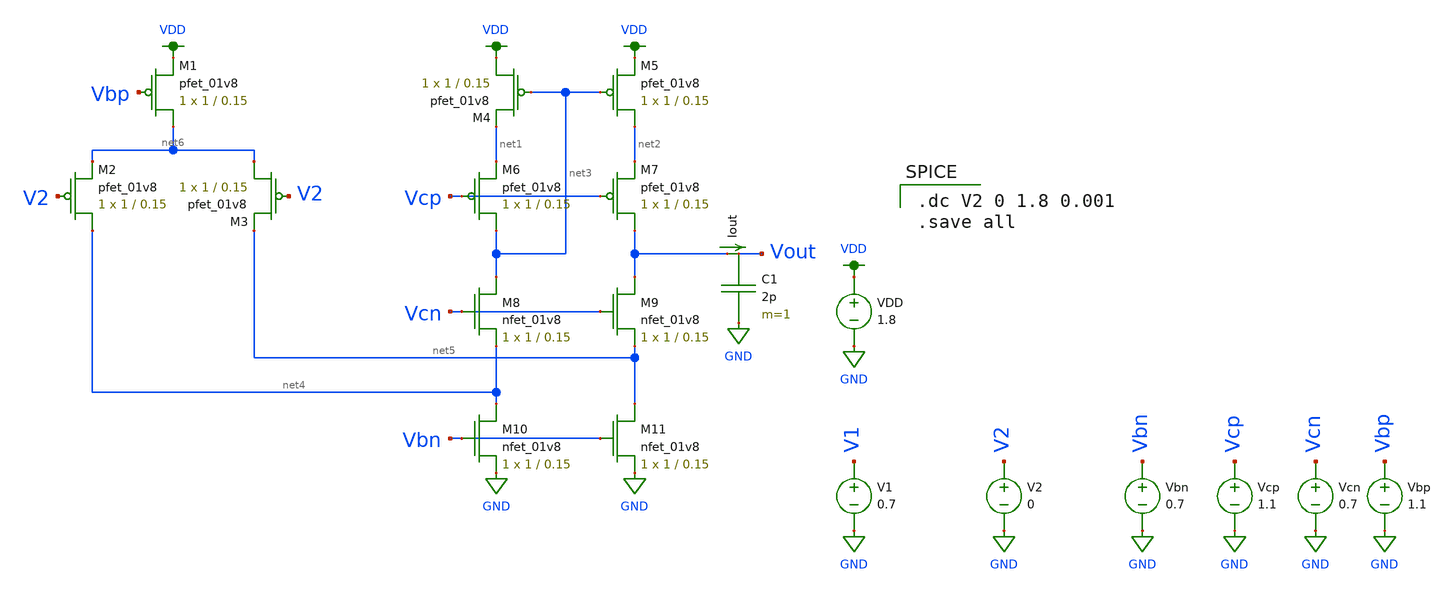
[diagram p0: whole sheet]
** sch_path: schematic/folded_cascode_differential_amplifier (copy).sch
**.subckt folded_cascode_differential_amplifier (copy)
XM1 net6 Vbp VDD VDD sky130_fd_pr__pfet_01v8 L=0.15 W=1 nf=1 ad='int((nf+1)/2) * W/nf * 0.29' as='int((nf+2)/2) * W/nf * 0.29'
+ pd='2*int((nf+1)/2) * (W/nf + 0.29)' ps='2*int((nf+2)/2) * (W/nf + 0.29)' nrd='0.29 / W' nrs='0.29 / W'
+ sa=0 sb=0 sd=0 mult=1 m=1
XM2 net4 V2 net6 VDD sky130_fd_pr__pfet_01v8 L=0.15 W=1 nf=1 ad='int((nf+1)/2) * W/nf * 0.29' as='int((nf+2)/2) * W/nf * 0.29'
+ pd='2*int((nf+1)/2) * (W/nf + 0.29)' ps='2*int((nf+2)/2) * (W/nf + 0.29)' nrd='0.29 / W' nrs='0.29 / W'
+ sa=0 sb=0 sd=0 mult=1 m=1
XM3 net6 V2 net5 VDD sky130_fd_pr__pfet_01v8 L=0.15 W=1 nf=1 ad='int((nf+1)/2) * W/nf * 0.29' as='int((nf+2)/2) * W/nf * 0.29'
+ pd='2*int((nf+1)/2) * (W/nf + 0.29)' ps='2*int((nf+2)/2) * (W/nf + 0.29)' nrd='0.29 / W' nrs='0.29 / W'
+ sa=0 sb=0 sd=0 mult=1 m=1
XM4 VDD net3 net1 VDD sky130_fd_pr__pfet_01v8 L=0.15 W=1 nf=1 ad='int((nf+1)/2) * W/nf * 0.29' as='int((nf+2)/2) * W/nf * 0.29'
+ pd='2*int((nf+1)/2) * (W/nf + 0.29)' ps='2*int((nf+2)/2) * (W/nf + 0.29)' nrd='0.29 / W' nrs='0.29 / W'
+ sa=0 sb=0 sd=0 mult=1 m=1
XM5 net2 net3 VDD VDD sky130_fd_pr__pfet_01v8 L=0.15 W=1 nf=1 ad='int((nf+1)/2) * W/nf * 0.29' as='int((nf+2)/2) * W/nf * 0.29'
+ pd='2*int((nf+1)/2) * (W/nf + 0.29)' ps='2*int((nf+2)/2) * (W/nf + 0.29)' nrd='0.29 / W' nrs='0.29 / W'
+ sa=0 sb=0 sd=0 mult=1 m=1
XM6 net3 Vcp net1 VDD sky130_fd_pr__pfet_01v8 L=0.15 W=1 nf=1 ad='int((nf+1)/2) * W/nf * 0.29' as='int((nf+2)/2) * W/nf * 0.29'
+ pd='2*int((nf+1)/2) * (W/nf + 0.29)' ps='2*int((nf+2)/2) * (W/nf + 0.29)' nrd='0.29 / W' nrs='0.29 / W'
+ sa=0 sb=0 sd=0 mult=1 m=1
XM7 Vout Vcp net2 VDD sky130_fd_pr__pfet_01v8 L=0.15 W=1 nf=1 ad='int((nf+1)/2) * W/nf * 0.29' as='int((nf+2)/2) * W/nf * 0.29'
+ pd='2*int((nf+1)/2) * (W/nf + 0.29)' ps='2*int((nf+2)/2) * (W/nf + 0.29)' nrd='0.29 / W' nrs='0.29 / W'
+ sa=0 sb=0 sd=0 mult=1 m=1
XM8 net3 Vcn net4 GND sky130_fd_pr__nfet_01v8 L=0.15 W=1 nf=1 ad='int((nf+1)/2) * W/nf * 0.29' as='int((nf+2)/2) * W/nf * 0.29'
+ pd='2*int((nf+1)/2) * (W/nf + 0.29)' ps='2*int((nf+2)/2) * (W/nf + 0.29)' nrd='0.29 / W' nrs='0.29 / W'
+ sa=0 sb=0 sd=0 mult=1 m=1
XM9 Vout Vcn net5 GND sky130_fd_pr__nfet_01v8 L=0.15 W=1 nf=1 ad='int((nf+1)/2) * W/nf * 0.29' as='int((nf+2)/2) * W/nf * 0.29'
+ pd='2*int((nf+1)/2) * (W/nf + 0.29)' ps='2*int((nf+2)/2) * (W/nf + 0.29)' nrd='0.29 / W' nrs='0.29 / W'
+ sa=0 sb=0 sd=0 mult=1 m=1
XM10 net4 Vbn GND GND sky130_fd_pr__nfet_01v8 L=0.15 W=1 nf=1 ad='int((nf+1)/2) * W/nf * 0.29' as='int((nf+2)/2) * W/nf * 0.29'
+ pd='2*int((nf+1)/2) * (W/nf + 0.29)' ps='2*int((nf+2)/2) * (W/nf + 0.29)' nrd='0.29 / W' nrs='0.29 / W'
+ sa=0 sb=0 sd=0 mult=1 m=1
XM11 net5 Vbn GND GND sky130_fd_pr__nfet_01v8 L=0.15 W=1 nf=1 ad='int((nf+1)/2) * W/nf * 0.29' as='int((nf+2)/2) * W/nf * 0.29'
+ pd='2*int((nf+1)/2) * (W/nf + 0.29)' ps='2*int((nf+2)/2) * (W/nf + 0.29)' nrd='0.29 / W' nrs='0.29 / W'
+ sa=0 sb=0 sd=0 mult=1 m=1
VDD VDD GND 1.8
V1 V1 GND 0.7
C1 Vout GND 2p m=1
V2 V2 GND 0
Vbn Vbn GND 0.7
Vcp Vcp GND 1.1
Vcn Vcn GND 0.7
Vbp Vbp GND 1.1
Iout Vout Vout 0
.save i(iout)
**** begin user architecture code

.option wnflag=1
.lib ~/skywater/skywater-pdk/libraries/sky130_fd_pr_ngspice/latest/models/sky130.lib.spice tt


.dc V2 0 1.8 0.001
.save all

**** end user architecture code
**.ends
.GLOBAL VDD
.GLOBAL GND
.end
